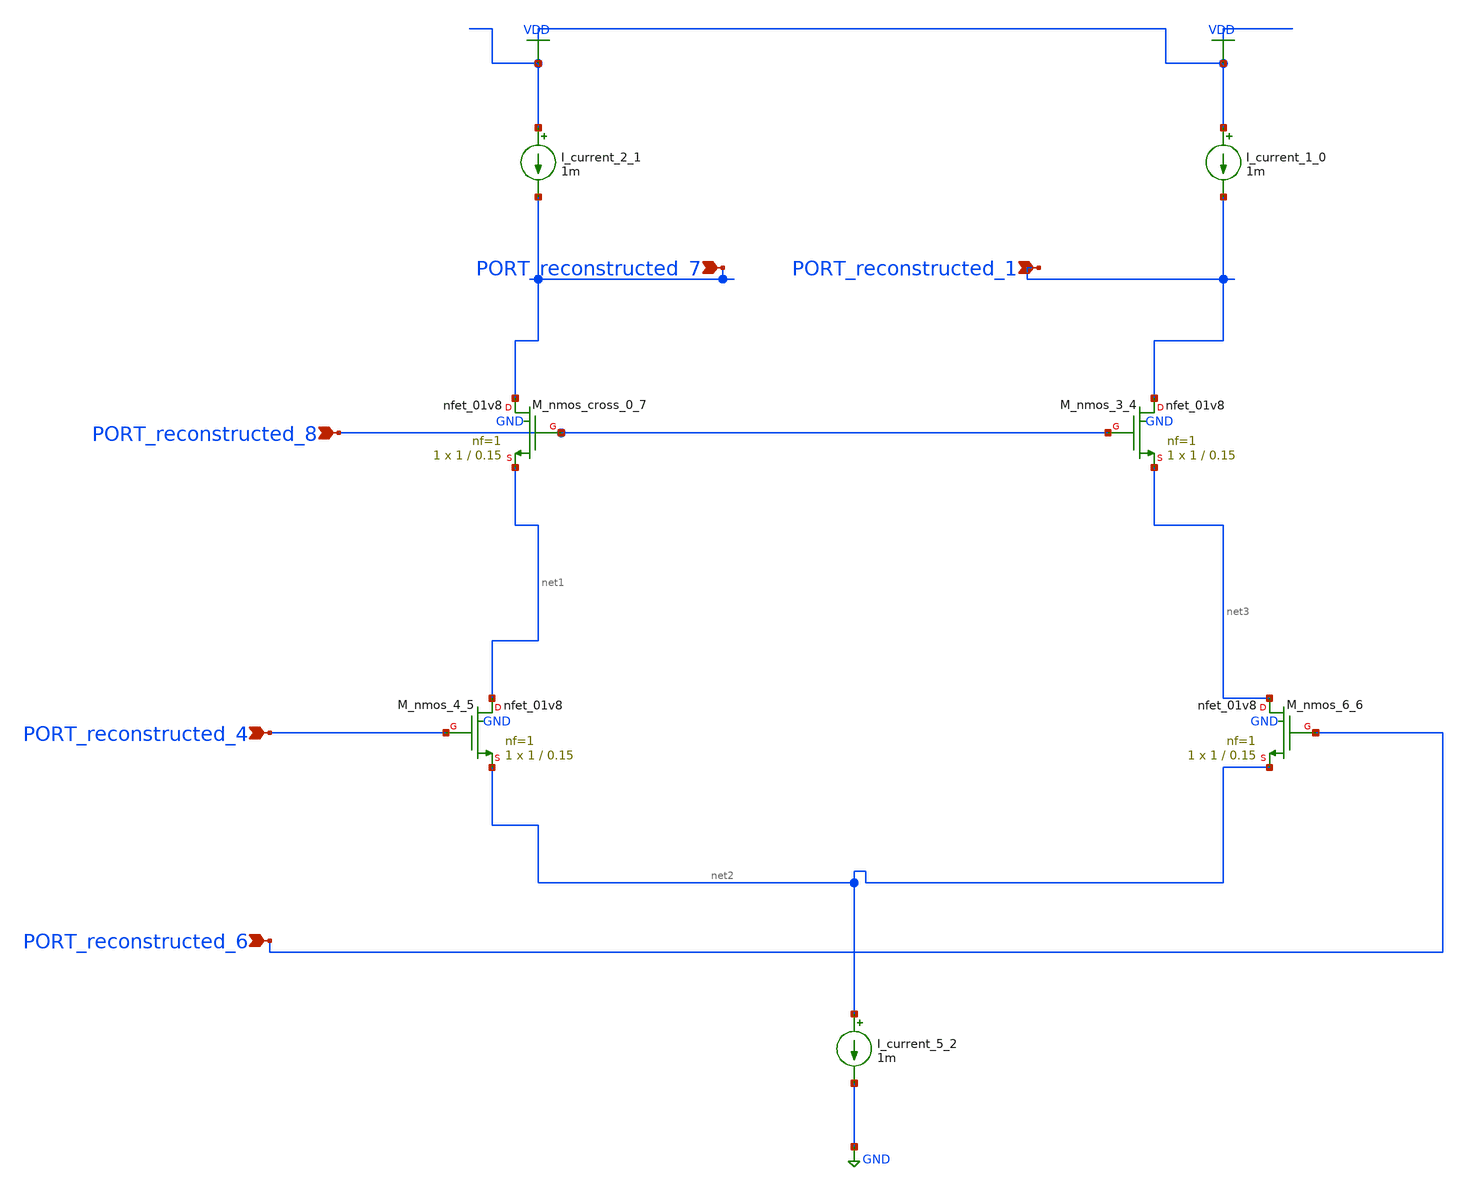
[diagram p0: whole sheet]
** sch_path: schematics/AMSNet/636.sch
**.subckt 636 PORT_reconstructed_7 PORT_reconstructed_4 PORT_reconstructed_6 PORT_reconstructed_8
*+ PORT_reconstructed_1
*.ipin PORT_reconstructed_7
*.ipin PORT_reconstructed_4
*.ipin PORT_reconstructed_6
*.ipin PORT_reconstructed_8
*.ipin PORT_reconstructed_1
I_current_1_0 VDD PORT_reconstructed_1 1m
I_current_2_1 VDD PORT_reconstructed_7 1m
I_current_5_2 net2 GND 1m
XM_nmos_3_4 PORT_reconstructed_1 PORT_reconstructed_8 net3 GND sky130_fd_pr__nfet_01v8 L=0.15 W=1 nf=1
+ ad='int((1 + 1)/2) * 1 / 1 * 0.29' as='int((1 + 2)/2) * 1 / 1 * 0.29' pd='2*int((1 + 1)/2) * (1 / 1 + 0.29)'
+ ps='2*int((1 + 2)/2) * (1 / 1 + 0.29)' nrd='0.29 / 1 ' nrs='0.29 / 1 ' sa=0 sb=0 sd=0 mult=1 m=1
XM_nmos_4_5 net1 PORT_reconstructed_4 net2 GND sky130_fd_pr__nfet_01v8 L=0.15 W=1 nf=1 ad='int((1 + 1)/2) * 1 / 1 * 0.29'
+ as='int((1 + 2)/2) * 1 / 1 * 0.29' pd='2*int((1 + 1)/2) * (1 / 1 + 0.29)' ps='2*int((1 + 2)/2) * (1 / 1 + 0.29)'
+ nrd='0.29 / 1 ' nrs='0.29 / 1 ' sa=0 sb=0 sd=0 mult=1 m=1
XM_nmos_6_6 net3 PORT_reconstructed_6 net2 GND sky130_fd_pr__nfet_01v8 L=0.15 W=1 nf=1 ad='int((1 + 1)/2) * 1 / 1 * 0.29'
+ as='int((1 + 2)/2) * 1 / 1 * 0.29' pd='2*int((1 + 1)/2) * (1 / 1 + 0.29)' ps='2*int((1 + 2)/2) * (1 / 1 + 0.29)'
+ nrd='0.29 / 1 ' nrs='0.29 / 1 ' sa=0 sb=0 sd=0 mult=1 m=1
XM_nmos_cross_0_7 PORT_reconstructed_7 PORT_reconstructed_8 net1 GND sky130_fd_pr__nfet_01v8 L=0.15 W=1
+ nf=1 ad='int((1 + 1)/2) * 1 / 1 * 0.29' as='int((1 + 2)/2) * 1 / 1 * 0.29' pd='2*int((1 + 1)/2) * (1 / 1 + 0.29)'
+ ps='2*int((1 + 2)/2) * (1 / 1 + 0.29)' nrd='0.29 / 1 ' nrs='0.29 / 1 ' sa=0 sb=0 sd=0 mult=1 m=1
**.ends
.GLOBAL GND
.GLOBAL VDD
.end
